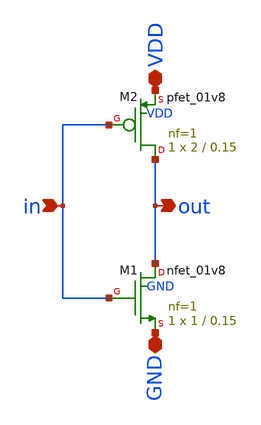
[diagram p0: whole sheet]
** sch_path: inverter/inv_lvs.sch
**.subckt inv_lvs in out VDD GND
*.ipin in
*.opin out
*.iopin VDD
*.iopin GND
XM1 out in GND GND sky130_fd_pr__nfet_01v8 L=0.15 W=1 nf=1 ad='int((1 + 1)/2) * 1 / 1 * 0.29' as='int((1 + 2)/2) * 1 / 1 * 0.29'
+ pd='2*int((1 + 1)/2) * (1 / 1 + 0.29)' ps='2*int((1 + 2)/2) * (1 / 1 + 0.29)' nrd='0.29 / 1 ' nrs='0.29 / 1 '
+ sa=0 sb=0 sd=0 mult=1 m=1
XM2 out in VDD VDD sky130_fd_pr__pfet_01v8 L=0.15 W=2 nf=1 ad='int((1 + 1)/2) * 2 / 1 * 0.29' as='int((1 + 2)/2) * 2 / 1 * 0.29'
+ pd='2*int((1 + 1)/2) * (2 / 1 + 0.29)' ps='2*int((1 + 2)/2) * (2 / 1 + 0.29)' nrd='0.29 / 2 ' nrs='0.29 / 2 '
+ sa=0 sb=0 sd=0 mult=1 m=1
**.ends
.end
